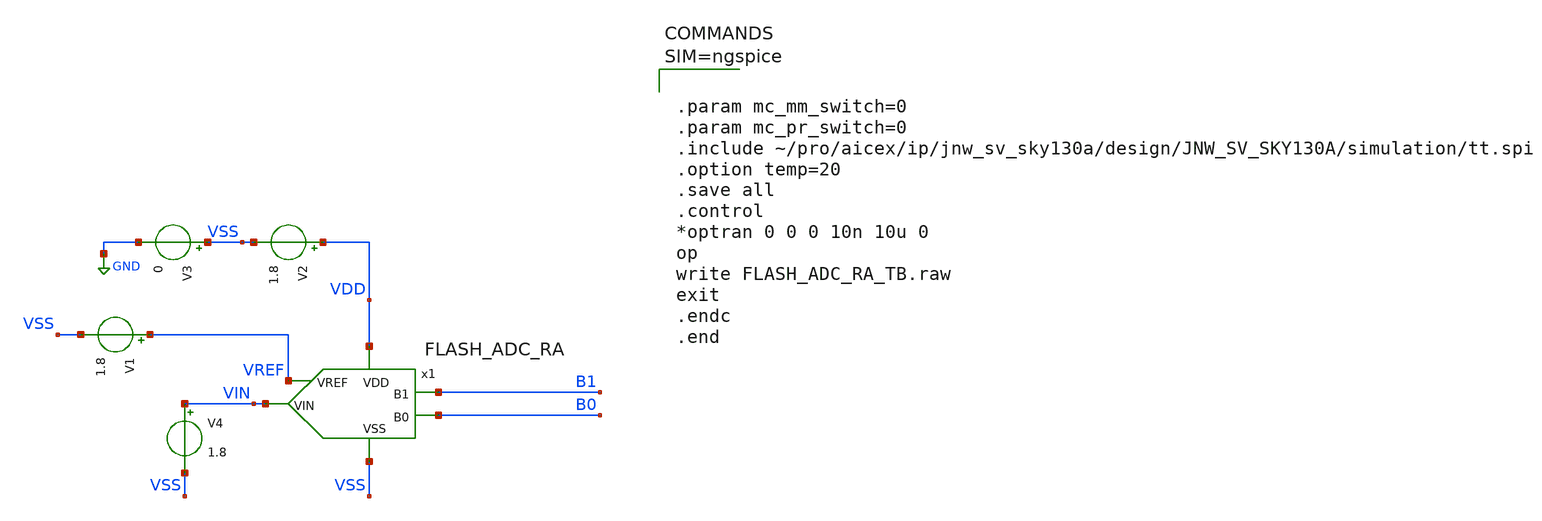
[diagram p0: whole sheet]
** sch_path: design/JNW_GR07_SKY130A/FLASH_ADC_RA_TB.sch
**.subckt FLASH_ADC_RA_TB
x1 VDD VIN VREF B1 B0 VSS FLASH_ADC_RA
V1 VREF VSS 1.8
V2 VDD VSS 1.8
V4 VIN VSS 1.8
V3 VSS GND 0
**** begin user architecture code



.param mc_mm_switch=0
.param mc_pr_switch=0
.include ~/pro/aicex/ip/jnw_sv_sky130a/design/JNW_SV_SKY130A/simulation/tt.spi
.option temp=20
.save all
.control
*optran 0 0 0 10n 10u 0
op
write FLASH_ADC_RA_TB.raw
exit
.endc
.end



**** end user architecture code
**.ends
.GLOBAL GND
.end
